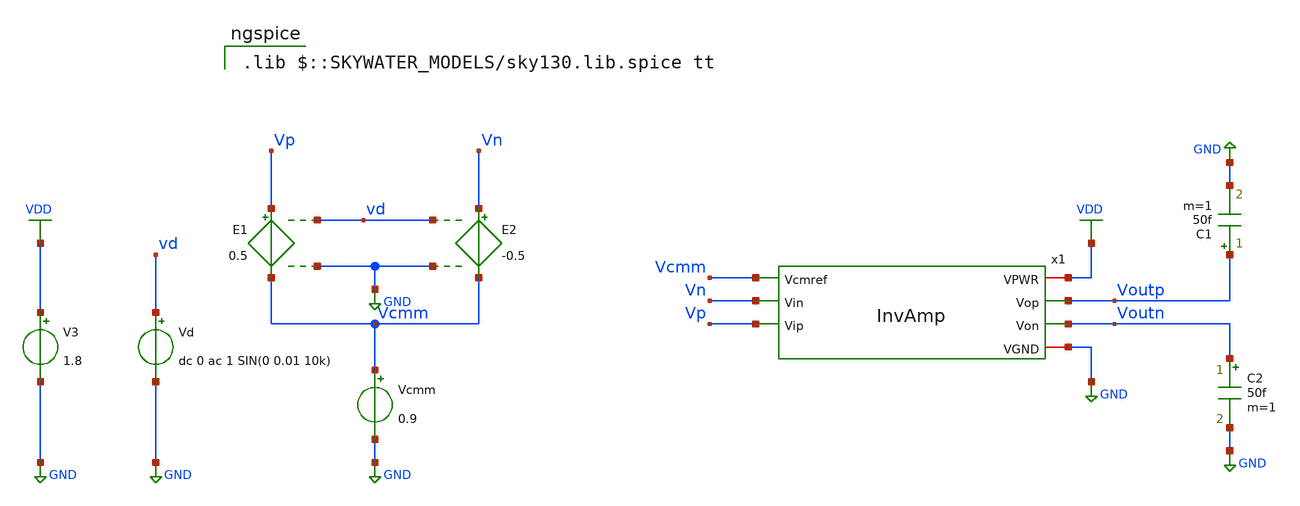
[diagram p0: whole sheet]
** sch_path: Circuits/Examples/InvAmp/InvAmp_tb.sch
**.subckt InvAmp_tb
V3 VDD GND 1.8
E1 Vp Vcmm vd GND 0.5
E2 Vn Vcmm vd GND -0.5
Vcmm Vcmm GND 0.9
Vd vd GND dc 0 ac 1 SIN(0 0.01 10k)
C2 Voutn GND 50f m=1
C1 Voutp GND 50f m=1
x1 VDD Vcmm Vn Voutp Voutn Vp GND InvAmp
**** begin user architecture code



* ngspice commands
.option savecurrents
.save all
.control
ac dec 1001 1 100Meg
let vod = V(Voutp)-V(Voutn)
meas ac gain max vod
let gain3dB = gain/sqrt(2)
meas ac BW TRIG at=1 TARG vod val=gain3dB fall=LAST
let GBW = BW*gain*1e-6
print GBW
print vodmax
plot vdb(vod) xlimit 1k 100Meg ylabel 'small signal gain'
let outd = 180/PI*cph(vod)
meas ac ftHz when vdb(vod)=1 fall=LAST
meas ac ph find outd when vdb(vod)=0 fall=LAST
let phm = ph+180
print phm
settype phase outd
plot outd xlimit 1k 100Meg ylabel 'phase'
tran 1u 1m
let vod = v(voutp)-v(voutn)
plot vod
op
.endc



 .lib $::SKYWATER_MODELS/sky130.lib.spice tt

**** end user architecture code
**.ends

* expanding   symbol:  /home/jakob/Documents/RALF/Circuits/Examples/InvAmp/InvAmp.sym # of pins=7
** sym_path: Circuits/Examples/InvAmp/InvAmp.sym
** sch_path: Circuits/Examples/InvAmp/InvAmp.sch
.subckt InvAmp VPWR Vcmref Vin Vop Von Vip VGND
*.iopin VPWR
*.iopin VGND
*.ipin Vcmref
*.ipin Vin
*.ipin Vip
*.opin Vop
*.opin Von
x1 VPWR Vcmref Vop Von vp vn VGND OpAmp
XR1 vp Vin VGND sky130_fd_pr__res_xhigh_po_0p35 L=1.75 mult=1 m=1
XR2 v1 vp VGND sky130_fd_pr__res_xhigh_po_0p35 L=1.75 mult=1 m=1
XR3 Von v1 VGND sky130_fd_pr__res_xhigh_po_0p35 L=1.75 mult=1 m=1
XR4 Vip vn VGND sky130_fd_pr__res_xhigh_po_0p35 L=1.75 mult=1 m=1
XR6 Vop v2 VGND sky130_fd_pr__res_xhigh_po_0p35 L=1.75 mult=1 m=1
XR5 v2 vn VGND sky130_fd_pr__res_xhigh_po_0p35 L=1.75 mult=1 m=1
.ends


* expanding   symbol:  /home/jakob/Documents/RALF/Circuits/Examples/OpAmp/OpAmp.sym # of pins=7
** sym_path: Circuits/Examples/OpAmp/OpAmp.sym
** sch_path: Circuits/Examples/OpAmp/OpAmp.sch
.subckt OpAmp VPWR Vcmref Vop Von Vp Vn VGND
*.opin Von
*.opin Vop
*.ipin Vcmref
*.ipin Vp
*.ipin Vn
*.iopin VPWR
*.iopin VGND
x2 VPWR Vcmref Von vcmfb Vop vbias VGND CMMFeedback
x3 VPWR vbias VGND GmBias
x1 VPWR Von vcmfb Vp Vn vbias vbias Vop VGND MillerOpAmp
.ends


* expanding   symbol:  /home/jakob/Documents/RALF/Circuits/Examples/OpAmp/CMMFeedback.sym # of
*+ pins=7
** sym_path: Circuits/Examples/OpAmp/CMMFeedback.sym
** sch_path: Circuits/Examples/OpAmp/CMMFeedback.sch
.subckt CMMFeedback Vdd Vcmref Vp Vout Vn Vbdan Vss
*.ipin Vbdan
*.opin Vout
*.ipin Vp
*.ipin Vcmref
*.ipin Vn
*.iopin Vss
*.iopin Vdd
XR1 Vp net1 Vss sky130_fd_pr__res_xhigh_po_0p35 L=3.5 mult=1 m=1
XR2 net1 net2 Vss sky130_fd_pr__res_xhigh_po_0p35 L=3.5 mult=1 m=1
XR3 net2 net3 Vss sky130_fd_pr__res_xhigh_po_0p35 L=3.5 mult=1 m=1
XR4 net3 net4 Vss sky130_fd_pr__res_xhigh_po_0p35 L=3.5 mult=1 m=1
XR5 net4 vcmi Vss sky130_fd_pr__res_xhigh_po_0p35 L=3.5 mult=1 m=1
XR6 Vn net5 Vss sky130_fd_pr__res_xhigh_po_0p35 L=3.5 mult=1 m=1
XR10 net5 net6 Vss sky130_fd_pr__res_xhigh_po_0p35 L=3.5 mult=1 m=1
XR9 net6 net7 Vss sky130_fd_pr__res_xhigh_po_0p35 L=3.5 mult=1 m=1
XR8 net7 net8 Vss sky130_fd_pr__res_xhigh_po_0p35 L=3.5 mult=1 m=1
XR7 net8 vcmi Vss sky130_fd_pr__res_xhigh_po_0p35 L=3.5 mult=1 m=1
x1 Vdd vdts Vout vdts Vcmref vcmi Vbdan Vss DiffAmp
.ends


* expanding   symbol:  /home/jakob/Documents/RALF/Circuits/Examples/OpAmp/GmBias.sym # of pins=3
** sym_path: Circuits/Examples/OpAmp/GmBias.sym
** sch_path: Circuits/Examples/OpAmp/GmBias.sch
.subckt GmBias Vdd Vbias Vss
*.opin Vbias
*.iopin Vss
*.iopin Vdd
XM6 Vbias Vbias Vss Vss sky130_fd_pr__nfet_01v8 L=2 W=1 nf=1 ad='int((nf+1)/2) * W/nf * 0.29' as='int((nf+2)/2) * W/nf * 0.29'
+ pd='2*int((nf+1)/2) * (W/nf + 0.29)' ps='2*int((nf+2)/2) * (W/nf + 0.29)' nrd='0.29 / W' nrs='0.29 / W'
+ sa=0 sb=0 sd=0 mult=1 m=1
XM2 v1 v1 Vdd Vdd sky130_fd_pr__pfet_01v8 L=1 W=4 nf=2 ad='int((nf+1)/2) * W/nf * 0.29' as='int((nf+2)/2) * W/nf * 0.29'
+ pd='2*int((nf+1)/2) * (W/nf + 0.29)' ps='2*int((nf+2)/2) * (W/nf + 0.29)' nrd='0.29 / W' nrs='0.29 / W'
+ sa=0 sb=0 sd=0 mult=1 m=1
XM1 Vbias v1 Vdd Vdd sky130_fd_pr__pfet_01v8 L=1 W=4 nf=2 ad='int((nf+1)/2) * W/nf * 0.29' as='int((nf+2)/2) * W/nf * 0.29'
+ pd='2*int((nf+1)/2) * (W/nf + 0.29)' ps='2*int((nf+2)/2) * (W/nf + 0.29)' nrd='0.29 / W' nrs='0.29 / W'
+ sa=0 sb=0 sd=0 mult=1 m=1
XM3 v1 Vbias net1 Vss sky130_fd_pr__nfet_01v8 L=2 W=1 nf=1 ad='int((nf+1)/2) * W/nf * 0.29' as='int((nf+2)/2) * W/nf * 0.29'
+ pd='2*int((nf+1)/2) * (W/nf + 0.29)' ps='2*int((nf+2)/2) * (W/nf + 0.29)' nrd='0.29 / W' nrs='0.29 / W'
+ sa=0 sb=0 sd=0 mult=1 m=1
XR6 Vss net1 Vss sky130_fd_pr__res_xhigh_po_0p35 L=1 mult=1 m=1
XM4 v1 v1 Vbias Vss sky130_fd_pr__nfet_01v8 L=2 W=1 nf=1 ad='int((nf+1)/2) * W/nf * 0.29' as='int((nf+2)/2) * W/nf * 0.29'
+ pd='2*int((nf+1)/2) * (W/nf + 0.29)' ps='2*int((nf+2)/2) * (W/nf + 0.29)' nrd='0.29 / W' nrs='0.29 / W'
+ sa=0 sb=0 sd=0 mult=1 m=1
.ends


* expanding   symbol:  /home/jakob/Documents/RALF/Circuits/Examples/OpAmp/MillerOpAmp.sym # of
*+ pins=9
** sym_path: Circuits/Examples/OpAmp/MillerOpAmp.sym
** sch_path: Circuits/Examples/OpAmp/MillerOpAmp.sch
.subckt MillerOpAmp VPWR Von Vbdap Vp Vn Vbdan Vbcsn Vop VGND
*.opin Von
*.opin Vop
*.ipin Vbcsn
*.ipin Vp
*.ipin Vn
*.ipin Vbdan
*.iopin VPWR
*.iopin VGND
*.ipin Vbdap
XC1 von1 Von sky130_fd_pr__cap_mim_m3_1 W=4 L=4 MF=1 m=1
XC2 vop1 Vop sky130_fd_pr__cap_mim_m3_1 W=4 L=4 MF=1 m=1
x1 VPWR Vbdap von1 vop1 Vp Vn Vbdan VGND DiffAmp
x2 VPWR von1 Von Vbcsn VGND CSAmp
x3 VPWR vop1 Vop Vbcsn VGND CSAmp
.ends


* expanding   symbol:  /home/jakob/Documents/RALF/Circuits/Examples/OpAmp/DiffAmp.sym # of pins=8
** sym_path: Circuits/Examples/OpAmp/DiffAmp.sym
** sch_path: Circuits/Examples/OpAmp/DiffAmp.sch
.subckt DiffAmp Vdd Vbp Von Vop Vp Vn Vbn Vss
*.iopin Vdd
*.iopin Vss
*.ipin Vp
*.ipin Vn
*.ipin Vbn
*.ipin Vbp
*.opin Vop
*.opin Von
XM1 Vop Vp vmid Vss sky130_fd_pr__nfet_01v8 L=1 W=1 nf=1 ad='int((nf+1)/2) * W/nf * 0.29' as='int((nf+2)/2) * W/nf * 0.29'
+ pd='2*int((nf+1)/2) * (W/nf + 0.29)' ps='2*int((nf+2)/2) * (W/nf + 0.29)' nrd='0.29 / W' nrs='0.29 / W'
+ sa=0 sb=0 sd=0 mult=1 m=1
XM2 Von Vn vmid Vss sky130_fd_pr__nfet_01v8 L=1 W=1 nf=1 ad='int((nf+1)/2) * W/nf * 0.29' as='int((nf+2)/2) * W/nf * 0.29'
+ pd='2*int((nf+1)/2) * (W/nf + 0.29)' ps='2*int((nf+2)/2) * (W/nf + 0.29)' nrd='0.29 / W' nrs='0.29 / W'
+ sa=0 sb=0 sd=0 mult=1 m=1
XM3 Vop Vbp Vdd Vdd sky130_fd_pr__pfet_01v8 L=1 W=2 nf=1 ad='int((nf+1)/2) * W/nf * 0.29' as='int((nf+2)/2) * W/nf * 0.29'
+ pd='2*int((nf+1)/2) * (W/nf + 0.29)' ps='2*int((nf+2)/2) * (W/nf + 0.29)' nrd='0.29 / W' nrs='0.29 / W'
+ sa=0 sb=0 sd=0 mult=1 m=1
XM4 Von Vbp Vdd Vdd sky130_fd_pr__pfet_01v8 L=1 W=2 nf=1 ad='int((nf+1)/2) * W/nf * 0.29' as='int((nf+2)/2) * W/nf * 0.29'
+ pd='2*int((nf+1)/2) * (W/nf + 0.29)' ps='2*int((nf+2)/2) * (W/nf + 0.29)' nrd='0.29 / W' nrs='0.29 / W'
+ sa=0 sb=0 sd=0 mult=1 m=1
XM5 vmid Vbn Vss Vss sky130_fd_pr__nfet_01v8 L=2 W=1 nf=1 ad='int((nf+1)/2) * W/nf * 0.29' as='int((nf+2)/2) * W/nf * 0.29'
+ pd='2*int((nf+1)/2) * (W/nf + 0.29)' ps='2*int((nf+2)/2) * (W/nf + 0.29)' nrd='0.29 / W' nrs='0.29 / W'
+ sa=0 sb=0 sd=0 mult=1 m=1
.ends


* expanding   symbol:  /home/jakob/Documents/RALF/Circuits/Examples/OpAmp/CSAmp.sym # of pins=5
** sym_path: Circuits/Examples/OpAmp/CSAmp.sym
** sch_path: Circuits/Examples/OpAmp/CSAmp.sch
.subckt CSAmp Vdd Vi Vo Vbn Vss
*.ipin Vbn
*.ipin Vi
*.iopin Vdd
*.iopin Vss
*.opin Vo
XM1 Vo Vi Vdd Vdd sky130_fd_pr__pfet_01v8 L=1 W=8 nf=1 ad='int((nf+1)/2) * W/nf * 0.29' as='int((nf+2)/2) * W/nf * 0.29'
+ pd='2*int((nf+1)/2) * (W/nf + 0.29)' ps='2*int((nf+2)/2) * (W/nf + 0.29)' nrd='0.29 / W' nrs='0.29 / W'
+ sa=0 sb=0 sd=0 mult=1 m=1
XM2 Vo Vbn Vss Vss sky130_fd_pr__nfet_01v8 L=2 W=10 nf=1 ad='int((nf+1)/2) * W/nf * 0.29' as='int((nf+2)/2) * W/nf * 0.29'
+ pd='2*int((nf+1)/2) * (W/nf + 0.29)' ps='2*int((nf+2)/2) * (W/nf + 0.29)' nrd='0.29 / W' nrs='0.29 / W'
+ sa=0 sb=0 sd=0 mult=1 m=1
XM3 Vo Vi Vdd Vdd sky130_fd_pr__pfet_01v8 L=1 W=8 nf=1 ad='int((nf+1)/2) * W/nf * 0.29' as='int((nf+2)/2) * W/nf * 0.29'
+ pd='2*int((nf+1)/2) * (W/nf + 0.29)' ps='2*int((nf+2)/2) * (W/nf + 0.29)' nrd='0.29 / W' nrs='0.29 / W'
+ sa=0 sb=0 sd=0 mult=1 m=1
XM4 Vo Vbn Vss Vss sky130_fd_pr__nfet_01v8 L=2 W=10 nf=1 ad='int((nf+1)/2) * W/nf * 0.29' as='int((nf+2)/2) * W/nf * 0.29'
+ pd='2*int((nf+1)/2) * (W/nf + 0.29)' ps='2*int((nf+2)/2) * (W/nf + 0.29)' nrd='0.29 / W' nrs='0.29 / W'
+ sa=0 sb=0 sd=0 mult=1 m=1
.ends

.GLOBAL GND
.GLOBAL VDD
.end
